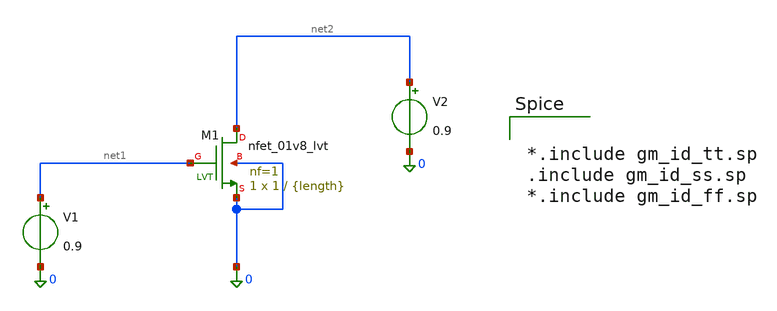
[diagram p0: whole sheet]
** sch_path: xschem/nmos/nmos_lvt_char.sch
**.subckt nmos_lvt_char
XM1 net2 net1 0 0 sky130_fd_pr__nfet_01v8_lvt L={length} W=1 nf=1 ad='int((1 + 1)/2) * 1 / 1 * 0.29'
+ as='int((1 + 2)/2) * 1 / 1 * 0.29' pd='2*int((1 + 1)/2) * (1 / 1 + 0.29)' ps='2*int((1 + 2)/2) * (1 / 1 + 0.29)'
+ nrd='0.29 / 1 ' nrs='0.29 / 1 ' sa=0 sb=0 sd=0 mult=1 m=1
V1 net1 0 0.9
V2 net2 0 0.9
**** begin user architecture code


*.include gm_id_tt.sp
.include gm_id_ss.sp
*.include gm_id_ff.sp


**** end user architecture code
**.ends
.end
